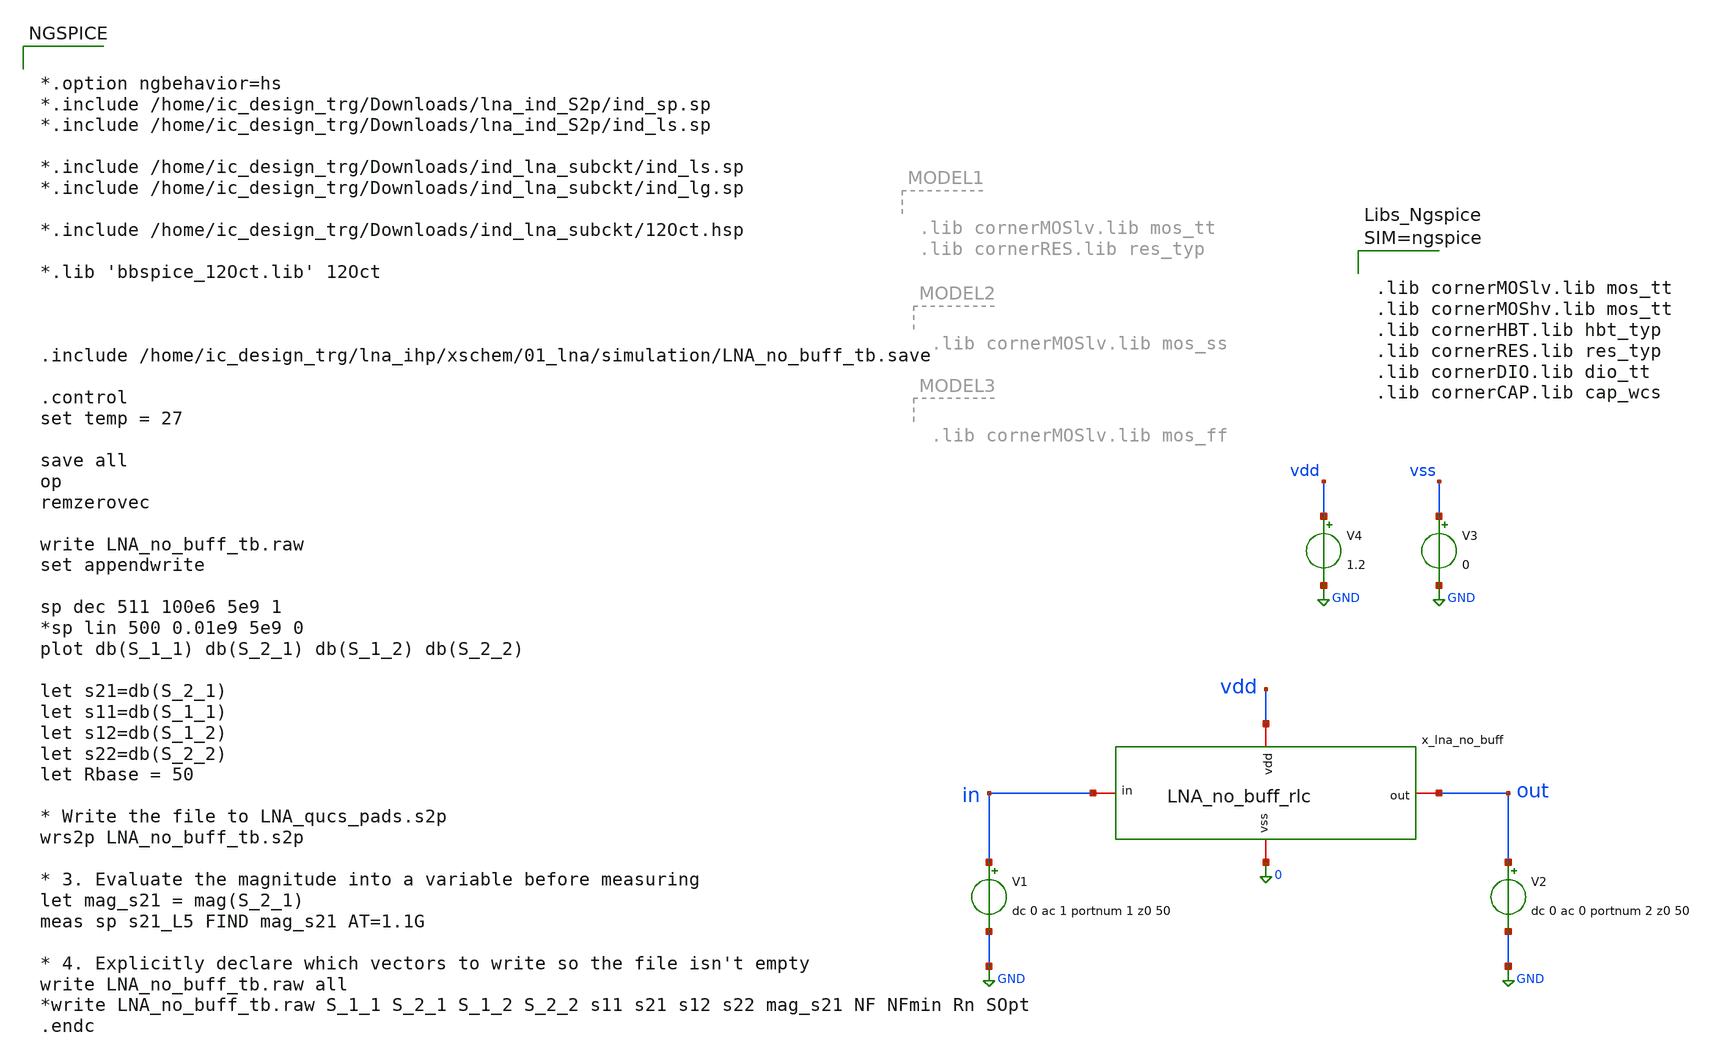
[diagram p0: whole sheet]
** sch_path: LNA7096-main/schematic/xschem/01_lna/LNA_no_buff_tb.sch
**.subckt LNA_no_buff_tb
V1 in GND dc 0 ac 1 portnum 1 z0 50
V2 out GND dc 0 ac 0 portnum 2 z0 50
V4 vdd GND 1.2
V3 vss GND 0
x_lna_no_buff vdd out in 0 LNA_no_buff_rlc
**** begin user architecture code


*.option ngbehavior=hs
*.include /home/ic_design_trg/Downloads/lna_ind_S2p/ind_sp.sp
*.include /home/ic_design_trg/Downloads/lna_ind_S2p/ind_ls.sp

*.include /home/ic_design_trg/Downloads/ind_lna_subckt/ind_ls.sp
*.include /home/ic_design_trg/Downloads/ind_lna_subckt/ind_lg.sp

*.include /home/ic_design_trg/Downloads/ind_lna_subckt/12Oct.hsp

*.lib 'bbspice_12Oct.lib' 12Oct



.include /home/ic_design_trg/lna_ihp/xschem/01_lna/simulation/LNA_no_buff_tb.save

.control
set temp = 27

save all
op
remzerovec

write LNA_no_buff_tb.raw
set appendwrite

sp dec 511 100e6 5e9 1
*sp lin 500 0.01e9 5e9 0
plot db(S_1_1) db(S_2_1) db(S_1_2) db(S_2_2)

let s21=db(S_2_1)
let s11=db(S_1_1)
let s12=db(S_1_2)
let s22=db(S_2_2)
let Rbase = 50

* Write the file to LNA_qucs_pads.s2p
wrs2p LNA_no_buff_tb.s2p

* 3. Evaluate the magnitude into a variable before measuring
let mag_s21 = mag(S_2_1)
meas sp s21_L5 FIND mag_s21 AT=1.1G

* 4. Explicitly declare which vectors to write so the file isn't empty
write LNA_no_buff_tb.raw all
*write LNA_no_buff_tb.raw S_1_1 S_2_1 S_1_2 S_2_2 s11 s21 s12 s22 mag_s21 NF NFmin Rn SOpt
.endc





.lib cornerMOSlv.lib mos_tt
.lib cornerMOShv.lib mos_tt
.lib cornerHBT.lib hbt_typ
.lib cornerRES.lib res_typ
.lib cornerDIO.lib dio_tt
.lib cornerCAP.lib cap_wcs



**** end user architecture code
**.ends

* expanding   symbol:  01_lna/LNA_no_buff_rlc.sym # of pins=4
** sym_path: LNA7096-main/schematic/xschem/01_lna/LNA_no_buff_rlc.sym
** sch_path: LNA7096-main/schematic/xschem/01_lna/LNA_no_buff_rlc.sch
.subckt LNA_no_buff_rlc vdd out in vss
*.iopin vdd
*.iopin vss
*.iopin in
*.iopin out
XR4 bias n4 vss rhigh w=1e-6 l=10e-6 m=1 b=0 mm_ok=1
XR5 vdd bias vss rhigh w=1e-6 l=7e-6 m=1 b=0 mm_ok=1
XC1 n1 out vss cap_rfcmim w=58e-6 l=59e-6 wfeed=5.0e-6 m=1 mm_ok=1
XM3 net1 n3 n2 vss sg13_lv_nmos w=5u l=0.25u ng=1 m=82 rfmode=1 mm_ok=1
XM5 n1 vdd net1 vss sg13_lv_nmos w=5u l=0.25u ng=1 m=82 rfmode=1 mm_ok=1
XM6 bias bias vss vss sg13_lv_nmos w=5u l=0.25u ng=1 m=1 rfmode=0 mm_ok=1
XC2 in n4 vss cap_rfcmim w=64.6e-6 l=62e-6 wfeed=5.0e-6 m=1 mm_ok=1
x1 n1 vdd vss ind_rlc Lser=18.1n Rser=9.8 Cshunt1=61.6f Rshunt1=2696 Cshunt2=62.2f Rshunt2=2774
x3 n2 vss vss ind_rlc Lser=1.381n Rser=1.339 Cshunt1=37f Rshunt1=2401 Cshunt2=38.5f Rshunt2=2353
x2 n4 n3 vss ind_rlc Lser=18.1n Rser=9.8 Cshunt1=61.6f Rshunt1=2696 Cshunt2=62.2f Rshunt2=2774
.ends


* expanding   symbol:  01_lna/13_oct_t-2_w-15_s-2_dia-168.sym # of pins=3
** sym_path: LNA7096-main/schematic/xschem/01_lna/ind_lg.sym
.include /home/ic_design_trg/lna_ihp/xschem/01_lna/lna_pads/simulation/ngspice_s2p/13_oct_t-2_w-15_s-2_dia-168.inc

* expanding   symbol:  01_lna/12_oct_t-4_w-14_s-2_dia-469_gds.sym # of pins=3
** sym_path: LNA7096-main/schematic/xschem/01_lna/ind_lg.sym
.include /home/ic_design_trg/lna_ihp/xschem/01_lna/lna_pads/simulation/ngspice_s2p/12_oct_t-4_w-14_s-2_dia-469_gds.inc

* expanding   symbol:  01_lna/ind_rlc.sym # of pins=3
** sym_path: LNA7096-main/schematic/xschem/01_lna/ind_rlc.sym
** sch_path: LNA7096-main/schematic/xschem/01_lna/ind_rlc.sch
.subckt ind_rlc p2 p1 vss  Lser=1n Rser=1k Rshunt1=1k Cshunt1=2p Rshunt2=1k Cshunt2=2p
*.iopin p1
*.iopin p2
*.iopin vss
L1 net2 p1 'Lser' m=1
R1 net2 p2 'Rser' m=1
R2 p1 net1 'Rshunt1' m=1
C1 net1 vss 'Cshunt1' m=1
R5 p2 net3 'Rshunt2' m=1
C4 net3 vss 'Cshunt2' m=1
.ends

.GLOBAL GND
.end
